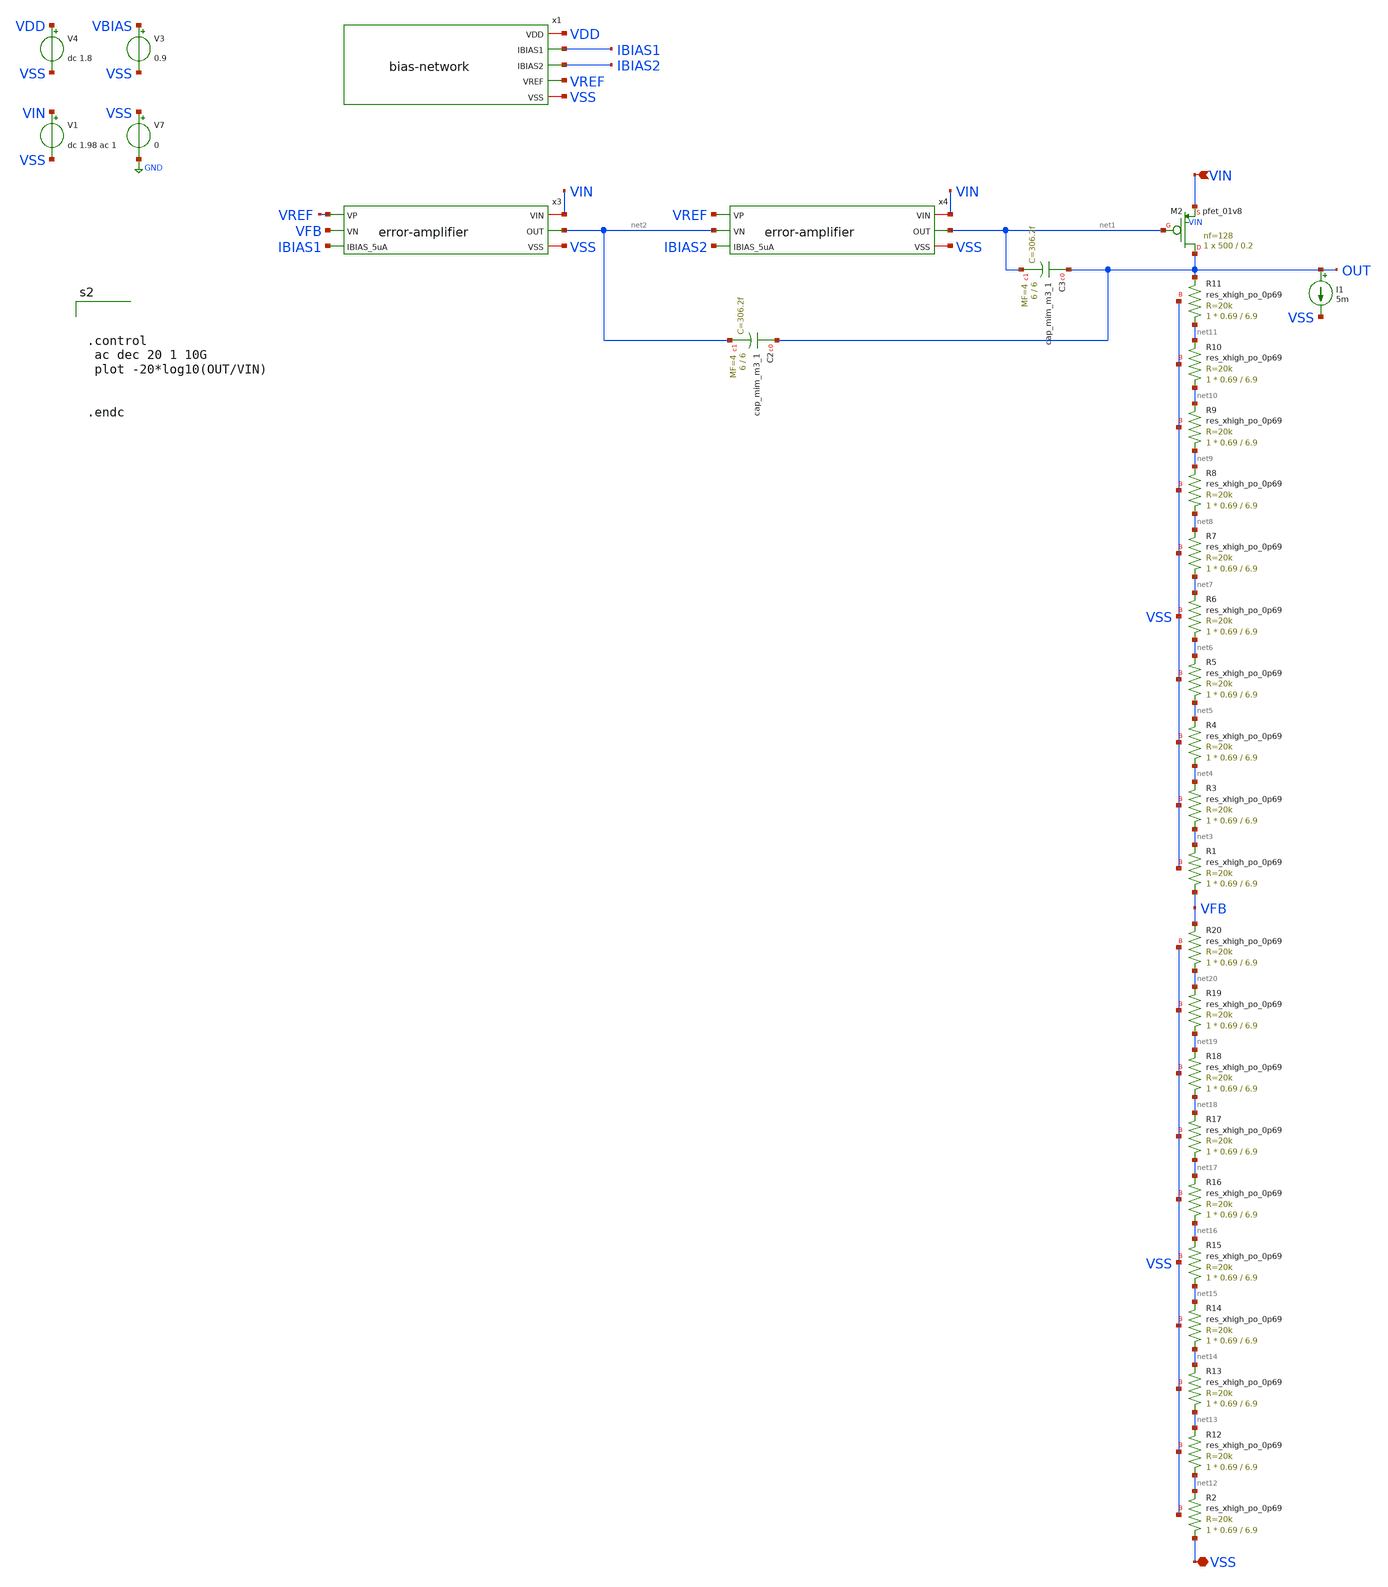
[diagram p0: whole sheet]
** sch_path: xschem/ldo_andriansyah/testbench/psrr.sch
**.subckt psrr VIN VSS
*.ipin VIN
*.iopin VSS
V7 VSS GND 0
V1 VIN VSS dc 1.98 ac 1
V3 VBIAS VSS 0.9
I1 OUT VSS 5m
XC2 OUT net2 sky130_fd_pr__cap_mim_m3_1 W=6 L=6 MF=4 m=4
XC3 OUT net1 sky130_fd_pr__cap_mim_m3_1 W=6 L=6 MF=4 m=4
x3 VIN VREF VFB IBIAS1 net2 VSS error-amplifier
XR1 VFB net3 VSS sky130_fd_pr__res_xhigh_po_0p69 L=6.9 mult=1 m=1
XM2 OUT net1 VIN VIN sky130_fd_pr__pfet_01v8 L=0.2 W=500 nf=128 ad='int((nf+1)/2) * W/nf * 0.29' as='int((nf+2)/2) * W/nf * 0.29'
+ pd='2*int((nf+1)/2) * (W/nf + 0.29)' ps='2*int((nf+2)/2) * (W/nf + 0.29)' nrd='0.29 / W' nrs='0.29 / W'
+ sa=0 sb=0 sd=0 mult=1 m=1
x4 VIN VREF net2 IBIAS2 net1 VSS error-amplifier
x1 VDD IBIAS1 IBIAS2 VREF VSS bias-network
V4 VDD VSS dc 1.8
XR3 net3 net4 VSS sky130_fd_pr__res_xhigh_po_0p69 L=6.9 mult=1 m=1
XR4 net4 net5 VSS sky130_fd_pr__res_xhigh_po_0p69 L=6.9 mult=1 m=1
XR5 net5 net6 VSS sky130_fd_pr__res_xhigh_po_0p69 L=6.9 mult=1 m=1
XR6 net6 net7 VSS sky130_fd_pr__res_xhigh_po_0p69 L=6.9 mult=1 m=1
XR7 net7 net8 VSS sky130_fd_pr__res_xhigh_po_0p69 L=6.9 mult=1 m=1
XR8 net8 net9 VSS sky130_fd_pr__res_xhigh_po_0p69 L=6.9 mult=1 m=1
XR9 net9 net10 VSS sky130_fd_pr__res_xhigh_po_0p69 L=6.9 mult=1 m=1
XR10 net10 net11 VSS sky130_fd_pr__res_xhigh_po_0p69 L=6.9 mult=1 m=1
XR11 net11 OUT VSS sky130_fd_pr__res_xhigh_po_0p69 L=6.9 mult=1 m=1
XR2 VSS net12 VSS sky130_fd_pr__res_xhigh_po_0p69 L=6.9 mult=1 m=1
XR12 net12 net13 VSS sky130_fd_pr__res_xhigh_po_0p69 L=6.9 mult=1 m=1
XR13 net13 net14 VSS sky130_fd_pr__res_xhigh_po_0p69 L=6.9 mult=1 m=1
XR14 net14 net15 VSS sky130_fd_pr__res_xhigh_po_0p69 L=6.9 mult=1 m=1
XR15 net15 net16 VSS sky130_fd_pr__res_xhigh_po_0p69 L=6.9 mult=1 m=1
XR16 net16 net17 VSS sky130_fd_pr__res_xhigh_po_0p69 L=6.9 mult=1 m=1
XR17 net17 net18 VSS sky130_fd_pr__res_xhigh_po_0p69 L=6.9 mult=1 m=1
XR18 net18 net19 VSS sky130_fd_pr__res_xhigh_po_0p69 L=6.9 mult=1 m=1
XR19 net19 net20 VSS sky130_fd_pr__res_xhigh_po_0p69 L=6.9 mult=1 m=1
XR20 net20 VFB VSS sky130_fd_pr__res_xhigh_po_0p69 L=6.9 mult=1 m=1
**** begin user architecture code

** opencircuitdesign pdks install
.lib $::SKYWATER_MODELS/sky130.lib.spice tt





.control
 ac dec 20 1 10G
 plot -20*log10(OUT/VIN)


.endc




**** end user architecture code
**.ends

* expanding   symbol:
*+  /foss/designs/2026/tt_sky26b_ldo_andriansyah/xschem/error-amplifier/error-amplifier.sym # of pins=6
** sym_path: xschem/error-amplifier/error-amplifier.sym
** sch_path: xschem/error-amplifier/error-amplifier.sch
.subckt error-amplifier VIN VP VN IBIAS_5uA OUT VSS
*.ipin IBIAS_5uA
*.ipin VN
*.ipin VP
*.iopin VIN
*.iopin VSS
*.opin OUT
XM1 net2 net2 VSS VSS sky130_fd_pr__nfet_01v8 L=0.6 W=4.2 nf=4 ad='int((nf+1)/2) * W/nf * 0.29' as='int((nf+2)/2) * W/nf * 0.29'
+ pd='2*int((nf+1)/2) * (W/nf + 0.29)' ps='2*int((nf+2)/2) * (W/nf + 0.29)' nrd='0.29 / W' nrs='0.29 / W'
+ sa=0 sb=0 sd=0 mult=1 m=1
XM2 OUT net2 VSS VSS sky130_fd_pr__nfet_01v8 L=0.6 W=4.2 nf=4 ad='int((nf+1)/2) * W/nf * 0.29' as='int((nf+2)/2) * W/nf * 0.29'
+ pd='2*int((nf+1)/2) * (W/nf + 0.29)' ps='2*int((nf+2)/2) * (W/nf + 0.29)' nrd='0.29 / W' nrs='0.29 / W'
+ sa=0 sb=0 sd=0 mult=1 m=1
XM3 net2 VN net1 VDD sky130_fd_pr__pfet_01v8 L=0.6 W=14 nf=4 ad='int((nf+1)/2) * W/nf * 0.29' as='int((nf+2)/2) * W/nf * 0.29'
+ pd='2*int((nf+1)/2) * (W/nf + 0.29)' ps='2*int((nf+2)/2) * (W/nf + 0.29)' nrd='0.29 / W' nrs='0.29 / W'
+ sa=0 sb=0 sd=0 mult=2 m=2
XM4 OUT VP net1 VDD sky130_fd_pr__pfet_01v8 L=0.6 W=14 nf=4 ad='int((nf+1)/2) * W/nf * 0.29' as='int((nf+2)/2) * W/nf * 0.29'
+ pd='2*int((nf+1)/2) * (W/nf + 0.29)' ps='2*int((nf+2)/2) * (W/nf + 0.29)' nrd='0.29 / W' nrs='0.29 / W'
+ sa=0 sb=0 sd=0 mult=2 m=2
XM5 net1 IBIAS_5uA VIN VIN sky130_fd_pr__pfet_01v8 L=0.6 W=6.6 nf=4 ad='int((nf+1)/2) * W/nf * 0.29'
+ as='int((nf+2)/2) * W/nf * 0.29' pd='2*int((nf+1)/2) * (W/nf + 0.29)' ps='2*int((nf+2)/2) * (W/nf + 0.29)'
+ nrd='0.29 / W' nrs='0.29 / W' sa=0 sb=0 sd=0 mult=1 m=1
XM6 IBIAS_5uA IBIAS_5uA VIN VIN sky130_fd_pr__pfet_01v8 L=0.6 W=6.6 nf=4 ad='int((nf+1)/2) * W/nf * 0.29'
+ as='int((nf+2)/2) * W/nf * 0.29' pd='2*int((nf+1)/2) * (W/nf + 0.29)' ps='2*int((nf+2)/2) * (W/nf + 0.29)'
+ nrd='0.29 / W' nrs='0.29 / W' sa=0 sb=0 sd=0 mult=1 m=1
.ends


* expanding   symbol:
*+  /foss/designs/2026/tt_sky26b_ldo_andriansyah/xschem/bias-net/schematics/bias-network.sym # of pins=5
** sym_path: xschem/bias-net/schematics/bias-network.sym
** sch_path: xschem/bias-net/schematics/bias-network.sch
.subckt bias-network VDD IBIAS1 IBIAS2 VREF VSS
*.iopin VDD
*.iopin VSS
*.opin IBIAS1
*.opin IBIAS2
*.opin VREF
XM2 VREF VREF VSS VSS sky130_fd_pr__nfet_01v8 L=2 W=3 nf=4 ad='int((nf+1)/2) * W/nf * 0.29' as='int((nf+2)/2) * W/nf * 0.29'
+ pd='2*int((nf+1)/2) * (W/nf + 0.29)' ps='2*int((nf+2)/2) * (W/nf + 0.29)' nrd='0.29 / W' nrs='0.29 / W'
+ sa=0 sb=0 sd=0 mult=2 m=2
XR1 VREF net1 VSS sky130_fd_pr__res_xhigh_po_0p69 L=6.9 mult=1 m=1
XR2 net2 net1 VSS sky130_fd_pr__res_xhigh_po_0p69 L=6.9 mult=1 m=1
XR3 net2 net3 VSS sky130_fd_pr__res_xhigh_po_0p69 L=6.9 mult=1 m=1
XR4 net4 net3 VSS sky130_fd_pr__res_xhigh_po_0p69 L=6.9 mult=1 m=1
XR5 net4 net5 VSS sky130_fd_pr__res_xhigh_po_0p69 L=6.9 mult=1 m=1
XR6 net9 net10 VSS sky130_fd_pr__res_xhigh_po_0p69 L=6.9 mult=1 m=1
XR7 net9 net8 VSS sky130_fd_pr__res_xhigh_po_0p69 L=6.9 mult=1 m=1
XR8 net7 net8 VSS sky130_fd_pr__res_xhigh_po_0p69 L=6.9 mult=1 m=1
XR9 net7 net6 VSS sky130_fd_pr__res_xhigh_po_0p69 L=6.9 mult=1 m=1
XR10 net5 net6 VSS sky130_fd_pr__res_xhigh_po_0p69 L=6.9 mult=1 m=1
XM1 IBIAS1 VREF VSS VSS sky130_fd_pr__nfet_01v8 L=2 W=3 nf=4 ad='int((nf+1)/2) * W/nf * 0.29' as='int((nf+2)/2) * W/nf * 0.29'
+ pd='2*int((nf+1)/2) * (W/nf + 0.29)' ps='2*int((nf+2)/2) * (W/nf + 0.29)' nrd='0.29 / W' nrs='0.29 / W'
+ sa=0 sb=0 sd=0 mult=2 m=2
XM3 IBIAS2 VREF VSS VSS sky130_fd_pr__nfet_01v8 L=2 W=3 nf=4 ad='int((nf+1)/2) * W/nf * 0.29' as='int((nf+2)/2) * W/nf * 0.29'
+ pd='2*int((nf+1)/2) * (W/nf + 0.29)' ps='2*int((nf+2)/2) * (W/nf + 0.29)' nrd='0.29 / W' nrs='0.29 / W'
+ sa=0 sb=0 sd=0 mult=2 m=2
XR11 net10 net11 VSS sky130_fd_pr__res_xhigh_po_0p69 L=6.9 mult=1 m=1
XR12 net12 net11 VSS sky130_fd_pr__res_xhigh_po_0p69 L=6.9 mult=1 m=1
XR13 net12 net13 VSS sky130_fd_pr__res_xhigh_po_0p69 L=6.9 mult=1 m=1
XR14 net14 net13 VSS sky130_fd_pr__res_xhigh_po_0p69 L=6.9 mult=1 m=1
XR15 net14 net15 VSS sky130_fd_pr__res_xhigh_po_0p69 L=6.9 mult=1 m=1
XR16 net19 VDD VSS sky130_fd_pr__res_xhigh_po_0p69 L=6.9 mult=1 m=1
XR17 net19 net18 VSS sky130_fd_pr__res_xhigh_po_0p69 L=6.9 mult=1 m=1
XR18 net17 net18 VSS sky130_fd_pr__res_xhigh_po_0p69 L=6.9 mult=1 m=1
XR19 net17 net16 VSS sky130_fd_pr__res_xhigh_po_0p69 L=6.9 mult=1 m=1
XR20 net15 net16 VSS sky130_fd_pr__res_xhigh_po_0p69 L=6.9 mult=1 m=1
XR21 VSS VSS VSS sky130_fd_pr__res_xhigh_po_0p69 L=6.9 mult=1 m=1
XR22 VSS VSS VSS sky130_fd_pr__res_xhigh_po_0p69 L=6.9 mult=1 m=1
.ends

.GLOBAL GND
.end
